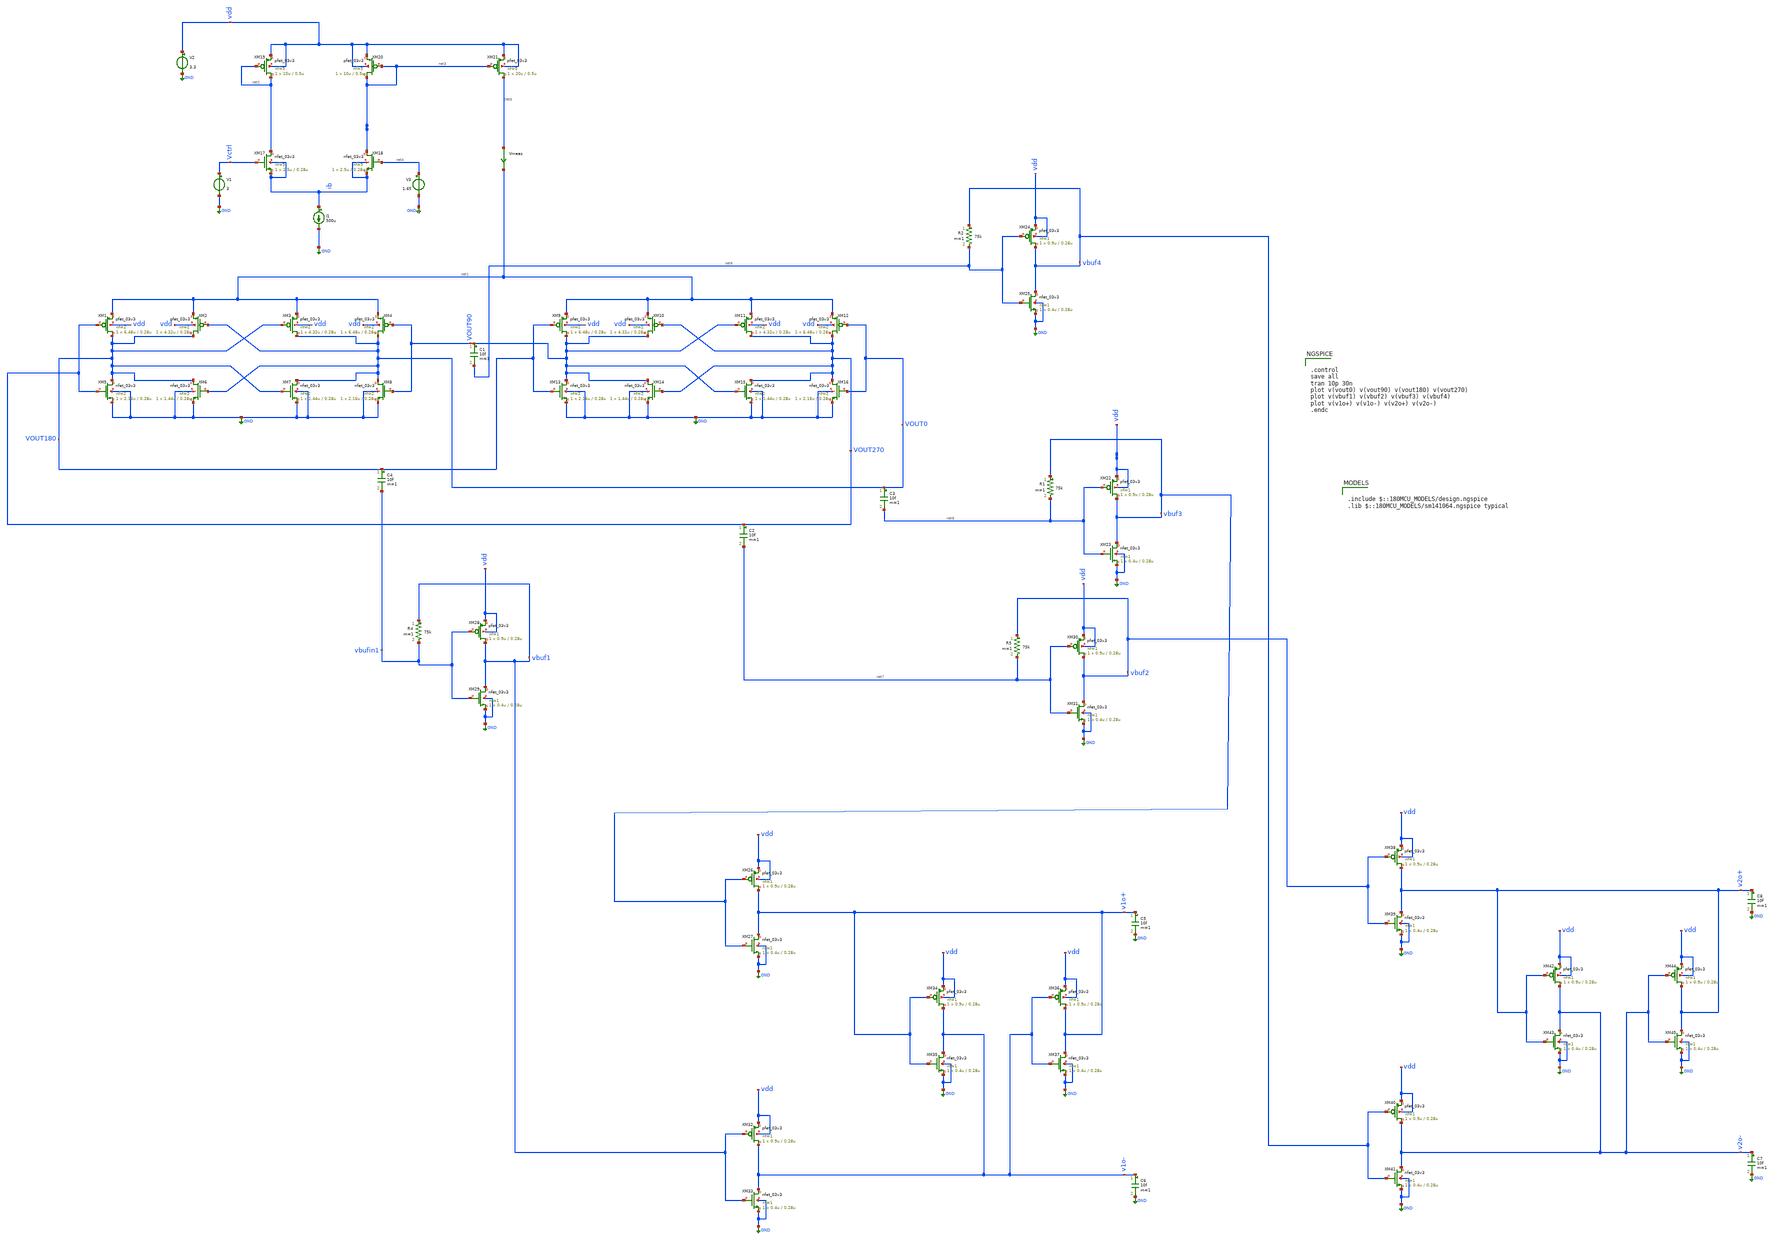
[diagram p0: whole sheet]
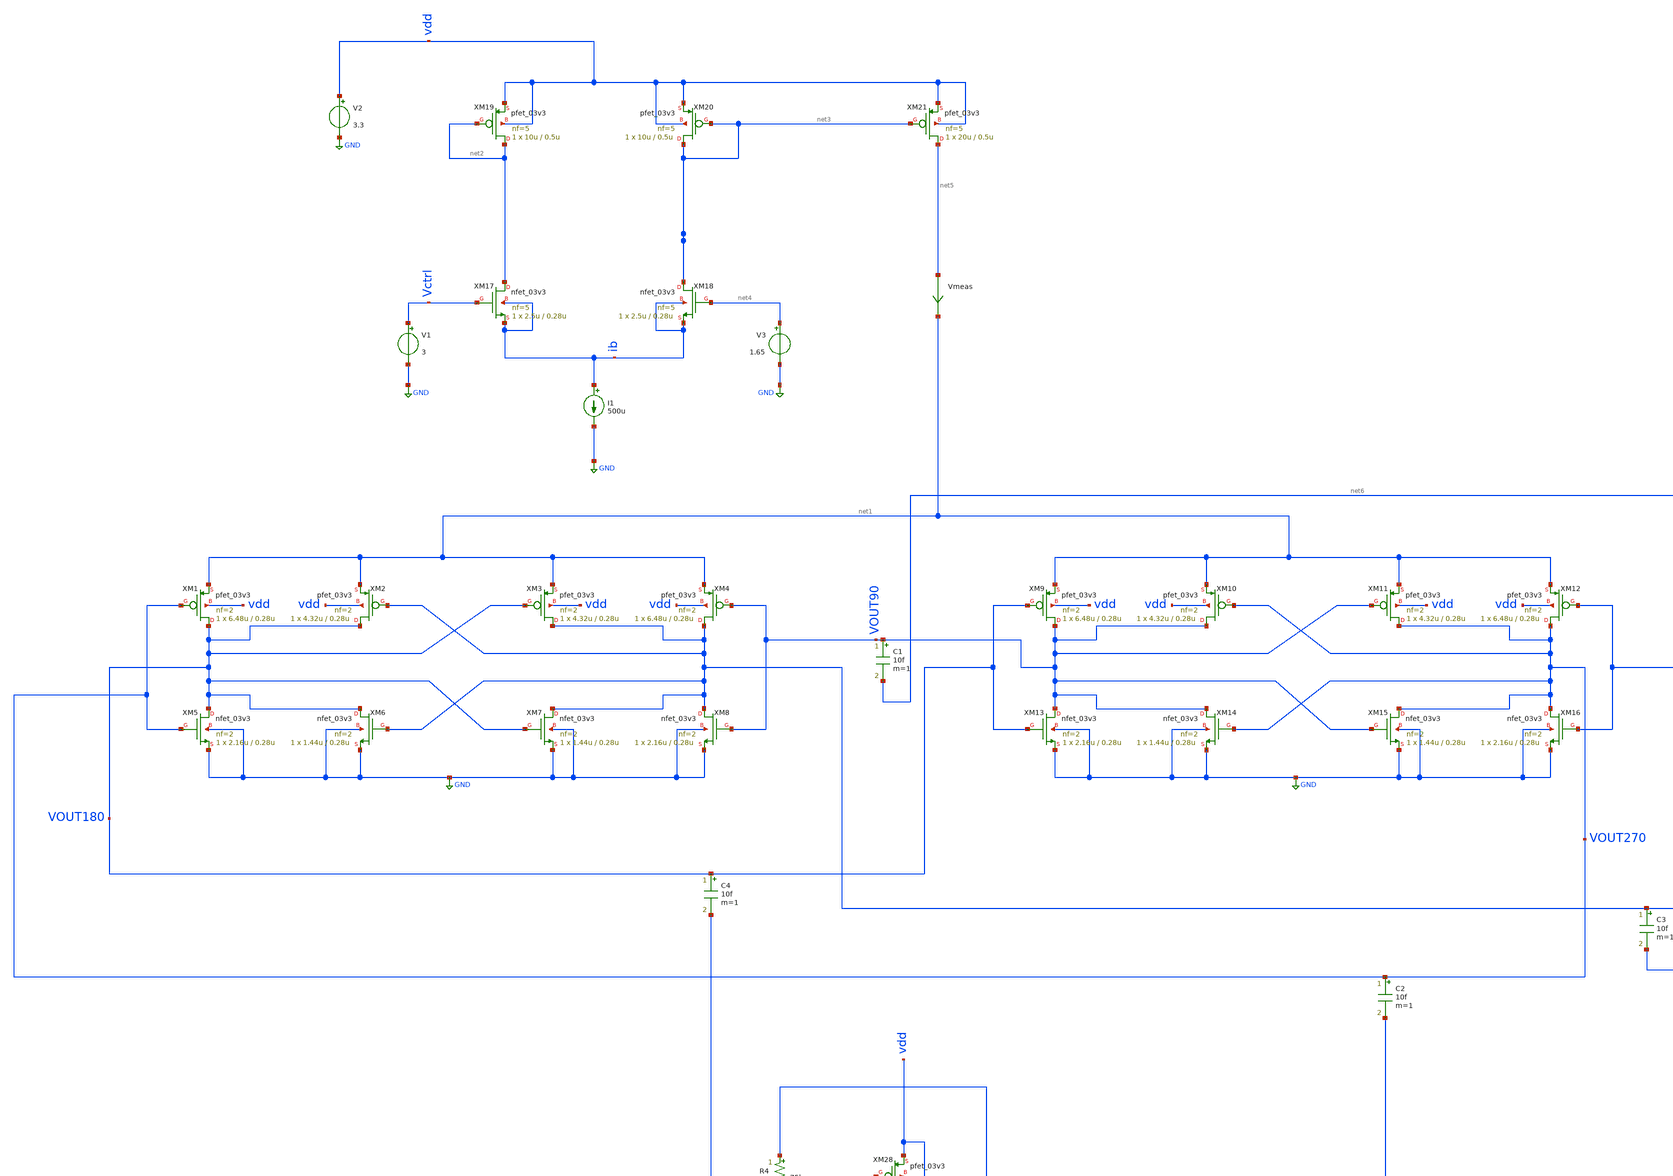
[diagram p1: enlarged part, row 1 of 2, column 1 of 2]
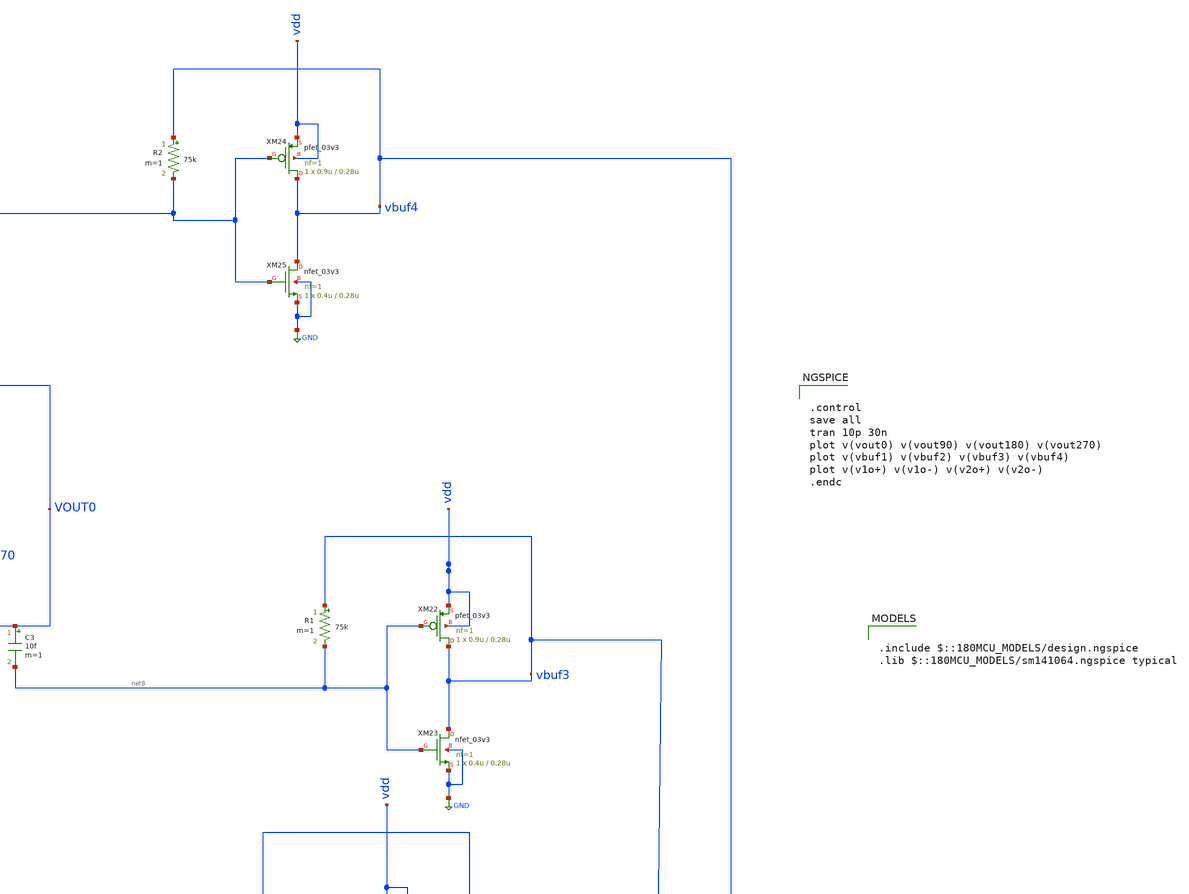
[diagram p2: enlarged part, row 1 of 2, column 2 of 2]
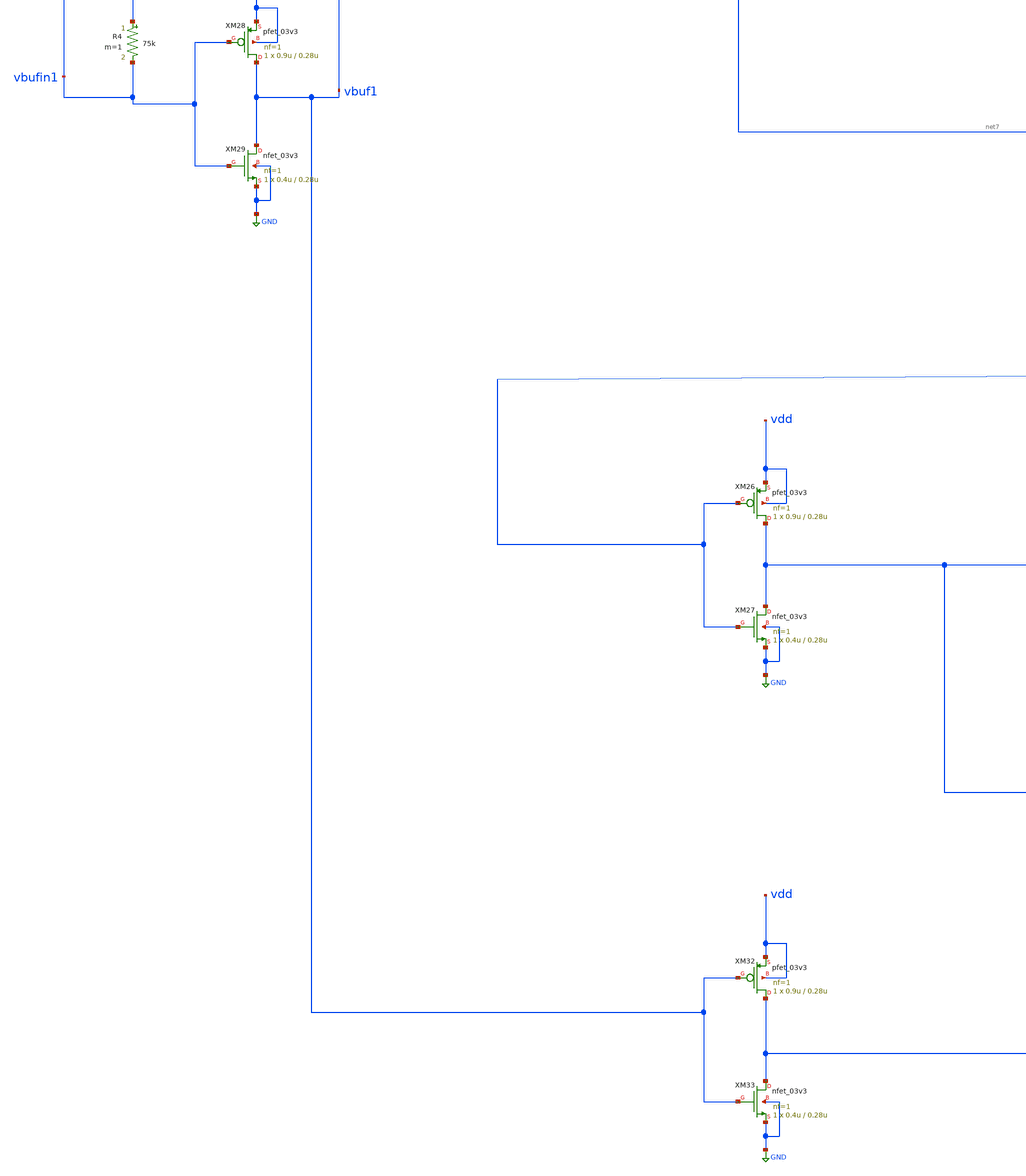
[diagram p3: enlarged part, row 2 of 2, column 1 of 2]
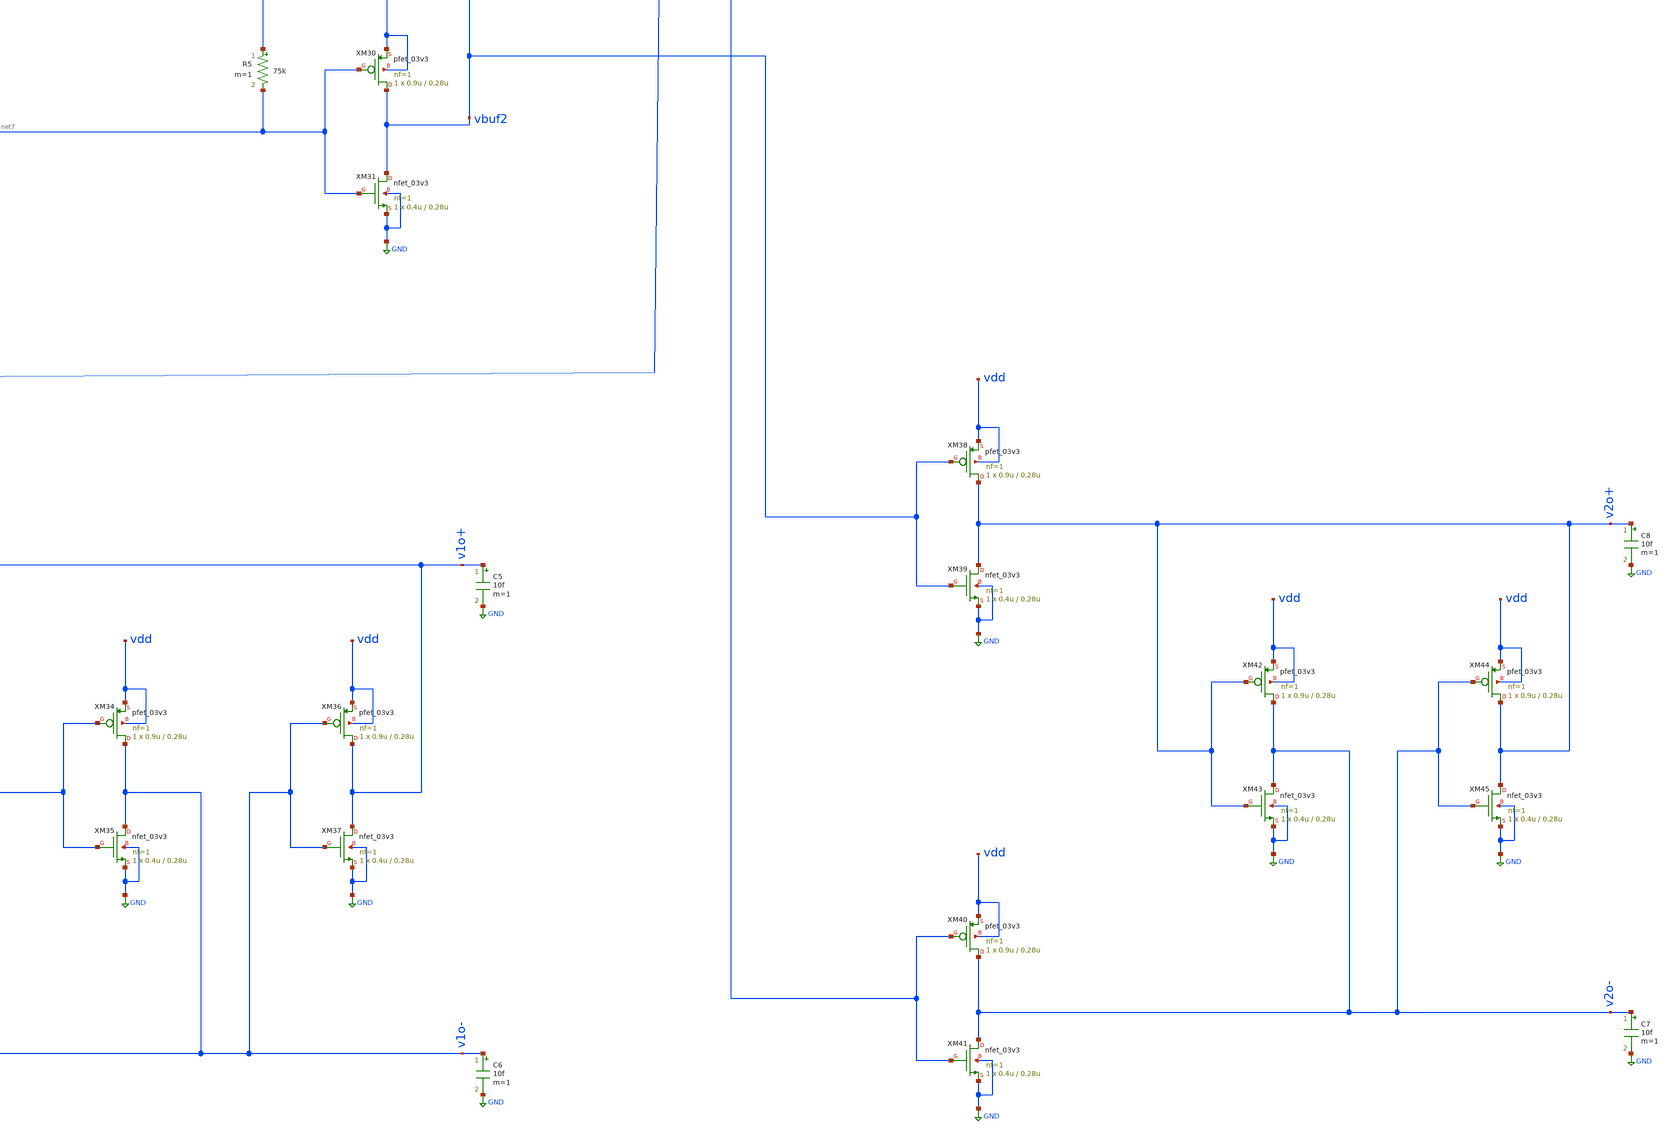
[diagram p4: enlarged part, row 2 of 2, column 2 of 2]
** sch_path: xschem/delay_tb.sch
**.subckt delay_tb
XM1 VOUT180 VOUT270 net1 vdd pfet_03v3 L=0.28u W=6.48u nf=2 ad='int((nf+1)/2) * W/nf * 0.18u' as='int((nf+2)/2) * W/nf * 0.18u'
+ pd='2*int((nf+1)/2) * (W/nf + 0.18u)' ps='2*int((nf+2)/2) * (W/nf + 0.18u)' nrd='0.18u / W' nrs='0.18u / W'
+ sa=0 sb=0 sd=0 m=1
XM2 VOUT180 VOUT0 net1 vdd pfet_03v3 L=0.28u W=4.32u nf=2 ad='int((nf+1)/2) * W/nf * 0.18u' as='int((nf+2)/2) * W/nf * 0.18u'
+ pd='2*int((nf+1)/2) * (W/nf + 0.18u)' ps='2*int((nf+2)/2) * (W/nf + 0.18u)' nrd='0.18u / W' nrs='0.18u / W'
+ sa=0 sb=0 sd=0 m=1
XM3 VOUT0 VOUT180 net1 vdd pfet_03v3 L=0.28u W=4.32u nf=2 ad='int((nf+1)/2) * W/nf * 0.18u' as='int((nf+2)/2) * W/nf * 0.18u'
+ pd='2*int((nf+1)/2) * (W/nf + 0.18u)' ps='2*int((nf+2)/2) * (W/nf + 0.18u)' nrd='0.18u / W' nrs='0.18u / W'
+ sa=0 sb=0 sd=0 m=1
XM4 VOUT0 VOUT90 net1 vdd pfet_03v3 L=0.28u W=6.48u nf=2 ad='int((nf+1)/2) * W/nf * 0.18u' as='int((nf+2)/2) * W/nf * 0.18u'
+ pd='2*int((nf+1)/2) * (W/nf + 0.18u)' ps='2*int((nf+2)/2) * (W/nf + 0.18u)' nrd='0.18u / W' nrs='0.18u / W'
+ sa=0 sb=0 sd=0 m=1
XM5 VOUT180 VOUT270 GND GND nfet_03v3 L=0.28u W=2.16u nf=2 ad='int((nf+1)/2) * W/nf * 0.18u' as='int((nf+2)/2) * W/nf * 0.18u'
+ pd='2*int((nf+1)/2) * (W/nf + 0.18u)' ps='2*int((nf+2)/2) * (W/nf + 0.18u)' nrd='0.18u / W' nrs='0.18u / W'
+ sa=0 sb=0 sd=0 m=1
XM6 VOUT180 VOUT0 GND GND nfet_03v3 L=0.28u W=1.44u nf=2 ad='int((nf+1)/2) * W/nf * 0.18u' as='int((nf+2)/2) * W/nf * 0.18u'
+ pd='2*int((nf+1)/2) * (W/nf + 0.18u)' ps='2*int((nf+2)/2) * (W/nf + 0.18u)' nrd='0.18u / W' nrs='0.18u / W'
+ sa=0 sb=0 sd=0 m=1
XM7 VOUT0 VOUT180 GND GND nfet_03v3 L=0.28u W=1.44u nf=2 ad='int((nf+1)/2) * W/nf * 0.18u' as='int((nf+2)/2) * W/nf * 0.18u'
+ pd='2*int((nf+1)/2) * (W/nf + 0.18u)' ps='2*int((nf+2)/2) * (W/nf + 0.18u)' nrd='0.18u / W' nrs='0.18u / W'
+ sa=0 sb=0 sd=0 m=1
XM8 VOUT0 VOUT90 GND GND nfet_03v3 L=0.28u W=2.16u nf=2 ad='int((nf+1)/2) * W/nf * 0.18u' as='int((nf+2)/2) * W/nf * 0.18u'
+ pd='2*int((nf+1)/2) * (W/nf + 0.18u)' ps='2*int((nf+2)/2) * (W/nf + 0.18u)' nrd='0.18u / W' nrs='0.18u / W'
+ sa=0 sb=0 sd=0 m=1
XM9 VOUT90 VOUT180 net1 vdd pfet_03v3 L=0.28u W=6.48u nf=2 ad='int((nf+1)/2) * W/nf * 0.18u' as='int((nf+2)/2) * W/nf * 0.18u'
+ pd='2*int((nf+1)/2) * (W/nf + 0.18u)' ps='2*int((nf+2)/2) * (W/nf + 0.18u)' nrd='0.18u / W' nrs='0.18u / W'
+ sa=0 sb=0 sd=0 m=1
XM10 VOUT90 VOUT270 net1 vdd pfet_03v3 L=0.28u W=4.32u nf=2 ad='int((nf+1)/2) * W/nf * 0.18u' as='int((nf+2)/2) * W/nf * 0.18u'
+ pd='2*int((nf+1)/2) * (W/nf + 0.18u)' ps='2*int((nf+2)/2) * (W/nf + 0.18u)' nrd='0.18u / W' nrs='0.18u / W'
+ sa=0 sb=0 sd=0 m=1
XM11 VOUT270 VOUT90 net1 vdd pfet_03v3 L=0.28u W=4.32u nf=2 ad='int((nf+1)/2) * W/nf * 0.18u' as='int((nf+2)/2) * W/nf * 0.18u'
+ pd='2*int((nf+1)/2) * (W/nf + 0.18u)' ps='2*int((nf+2)/2) * (W/nf + 0.18u)' nrd='0.18u / W' nrs='0.18u / W'
+ sa=0 sb=0 sd=0 m=1
XM12 VOUT270 VOUT0 net1 vdd pfet_03v3 L=0.28u W=6.48u nf=2 ad='int((nf+1)/2) * W/nf * 0.18u' as='int((nf+2)/2) * W/nf * 0.18u'
+ pd='2*int((nf+1)/2) * (W/nf + 0.18u)' ps='2*int((nf+2)/2) * (W/nf + 0.18u)' nrd='0.18u / W' nrs='0.18u / W'
+ sa=0 sb=0 sd=0 m=1
XM13 VOUT90 VOUT180 GND GND nfet_03v3 L=0.28u W=2.16u nf=2 ad='int((nf+1)/2) * W/nf * 0.18u' as='int((nf+2)/2) * W/nf * 0.18u'
+ pd='2*int((nf+1)/2) * (W/nf + 0.18u)' ps='2*int((nf+2)/2) * (W/nf + 0.18u)' nrd='0.18u / W' nrs='0.18u / W'
+ sa=0 sb=0 sd=0 m=1
XM14 VOUT90 VOUT270 GND GND nfet_03v3 L=0.28u W=1.44u nf=2 ad='int((nf+1)/2) * W/nf * 0.18u' as='int((nf+2)/2) * W/nf * 0.18u'
+ pd='2*int((nf+1)/2) * (W/nf + 0.18u)' ps='2*int((nf+2)/2) * (W/nf + 0.18u)' nrd='0.18u / W' nrs='0.18u / W'
+ sa=0 sb=0 sd=0 m=1
XM15 VOUT270 VOUT90 GND GND nfet_03v3 L=0.28u W=1.44u nf=2 ad='int((nf+1)/2) * W/nf * 0.18u' as='int((nf+2)/2) * W/nf * 0.18u'
+ pd='2*int((nf+1)/2) * (W/nf + 0.18u)' ps='2*int((nf+2)/2) * (W/nf + 0.18u)' nrd='0.18u / W' nrs='0.18u / W'
+ sa=0 sb=0 sd=0 m=1
XM16 VOUT270 VOUT0 GND GND nfet_03v3 L=0.28u W=2.16u nf=2 ad='int((nf+1)/2) * W/nf * 0.18u' as='int((nf+2)/2) * W/nf * 0.18u'
+ pd='2*int((nf+1)/2) * (W/nf + 0.18u)' ps='2*int((nf+2)/2) * (W/nf + 0.18u)' nrd='0.18u / W' nrs='0.18u / W'
+ sa=0 sb=0 sd=0 m=1
V1 Vctrl GND 3
V2 vdd GND 3.3
I1 ib GND 500u
V3 net4 GND 1.65
XM17 net2 Vctrl ib ib nfet_03v3 L=0.28u W=2.5u nf=5 ad='int((nf+1)/2) * W/nf * 0.18u' as='int((nf+2)/2) * W/nf * 0.18u'
+ pd='2*int((nf+1)/2) * (W/nf + 0.18u)' ps='2*int((nf+2)/2) * (W/nf + 0.18u)' nrd='0.18u / W' nrs='0.18u / W'
+ sa=0 sb=0 sd=0 m=1
XM18 net3 net4 ib ib nfet_03v3 L=0.28u W=2.5u nf=5 ad='int((nf+1)/2) * W/nf * 0.18u' as='int((nf+2)/2) * W/nf * 0.18u'
+ pd='2*int((nf+1)/2) * (W/nf + 0.18u)' ps='2*int((nf+2)/2) * (W/nf + 0.18u)' nrd='0.18u / W' nrs='0.18u / W'
+ sa=0 sb=0 sd=0 m=1
XM19 net2 net2 vdd vdd pfet_03v3 L=0.5u W=10u nf=5 ad='int((nf+1)/2) * W/nf * 0.18u' as='int((nf+2)/2) * W/nf * 0.18u'
+ pd='2*int((nf+1)/2) * (W/nf + 0.18u)' ps='2*int((nf+2)/2) * (W/nf + 0.18u)' nrd='0.18u / W' nrs='0.18u / W'
+ sa=0 sb=0 sd=0 m=1
XM20 net3 net3 vdd vdd pfet_03v3 L=0.5u W=10u nf=5 ad='int((nf+1)/2) * W/nf * 0.18u' as='int((nf+2)/2) * W/nf * 0.18u'
+ pd='2*int((nf+1)/2) * (W/nf + 0.18u)' ps='2*int((nf+2)/2) * (W/nf + 0.18u)' nrd='0.18u / W' nrs='0.18u / W'
+ sa=0 sb=0 sd=0 m=1
Vmeas net5 net1 0
.save i(vmeas)
XM21 net5 net3 vdd vdd pfet_03v3 L=0.5u W=20u nf=5 ad='int((nf+1)/2) * W/nf * 0.18u' as='int((nf+2)/2) * W/nf * 0.18u'
+ pd='2*int((nf+1)/2) * (W/nf + 0.18u)' ps='2*int((nf+2)/2) * (W/nf + 0.18u)' nrd='0.18u / W' nrs='0.18u / W'
+ sa=0 sb=0 sd=0 m=1
C1 VOUT90 net6 10f m=1
C2 VOUT270 net7 10f m=1
C3 VOUT0 net8 10f m=1
C4 VOUT180 vbufin1 10f m=1
XM28 vbuf1 vbufin1 vdd vdd pfet_03v3 L=0.28u W=0.9u nf=1 ad='int((nf+1)/2) * W/nf * 0.18u' as='int((nf+2)/2) * W/nf * 0.18u'
+ pd='2*int((nf+1)/2) * (W/nf + 0.18u)' ps='2*int((nf+2)/2) * (W/nf + 0.18u)' nrd='0.18u / W' nrs='0.18u / W'
+ sa=0 sb=0 sd=0 m=1
XM29 vbuf1 vbufin1 GND GND nfet_03v3 L=0.28u W=0.4u nf=1 ad='int((nf+1)/2) * W/nf * 0.18u' as='int((nf+2)/2) * W/nf * 0.18u'
+ pd='2*int((nf+1)/2) * (W/nf + 0.18u)' ps='2*int((nf+2)/2) * (W/nf + 0.18u)' nrd='0.18u / W' nrs='0.18u / W'
+ sa=0 sb=0 sd=0 m=1
R4 vbuf1 vbufin1 75k m=1
XM30 vbuf2 net7 vdd vdd pfet_03v3 L=0.28u W=0.9u nf=1 ad='int((nf+1)/2) * W/nf * 0.18u' as='int((nf+2)/2) * W/nf * 0.18u'
+ pd='2*int((nf+1)/2) * (W/nf + 0.18u)' ps='2*int((nf+2)/2) * (W/nf + 0.18u)' nrd='0.18u / W' nrs='0.18u / W'
+ sa=0 sb=0 sd=0 m=1
XM31 vbuf2 net7 GND GND nfet_03v3 L=0.28u W=0.4u nf=1 ad='int((nf+1)/2) * W/nf * 0.18u' as='int((nf+2)/2) * W/nf * 0.18u'
+ pd='2*int((nf+1)/2) * (W/nf + 0.18u)' ps='2*int((nf+2)/2) * (W/nf + 0.18u)' nrd='0.18u / W' nrs='0.18u / W'
+ sa=0 sb=0 sd=0 m=1
R5 vbuf2 net7 75k m=1
XM22 vbuf3 net8 vdd vdd pfet_03v3 L=0.28u W=0.9u nf=1 ad='int((nf+1)/2) * W/nf * 0.18u' as='int((nf+2)/2) * W/nf * 0.18u'
+ pd='2*int((nf+1)/2) * (W/nf + 0.18u)' ps='2*int((nf+2)/2) * (W/nf + 0.18u)' nrd='0.18u / W' nrs='0.18u / W'
+ sa=0 sb=0 sd=0 m=1
XM23 vbuf3 net8 GND GND nfet_03v3 L=0.28u W=0.4u nf=1 ad='int((nf+1)/2) * W/nf * 0.18u' as='int((nf+2)/2) * W/nf * 0.18u'
+ pd='2*int((nf+1)/2) * (W/nf + 0.18u)' ps='2*int((nf+2)/2) * (W/nf + 0.18u)' nrd='0.18u / W' nrs='0.18u / W'
+ sa=0 sb=0 sd=0 m=1
R1 vbuf3 net8 75k m=1
XM24 vbuf4 net6 vdd vdd pfet_03v3 L=0.28u W=0.9u nf=1 ad='int((nf+1)/2) * W/nf * 0.18u' as='int((nf+2)/2) * W/nf * 0.18u'
+ pd='2*int((nf+1)/2) * (W/nf + 0.18u)' ps='2*int((nf+2)/2) * (W/nf + 0.18u)' nrd='0.18u / W' nrs='0.18u / W'
+ sa=0 sb=0 sd=0 m=1
XM25 vbuf4 net6 GND GND nfet_03v3 L=0.28u W=0.4u nf=1 ad='int((nf+1)/2) * W/nf * 0.18u' as='int((nf+2)/2) * W/nf * 0.18u'
+ pd='2*int((nf+1)/2) * (W/nf + 0.18u)' ps='2*int((nf+2)/2) * (W/nf + 0.18u)' nrd='0.18u / W' nrs='0.18u / W'
+ sa=0 sb=0 sd=0 m=1
R2 vbuf4 net6 75k m=1
XM26 v1o+ vbuf3 vdd vdd pfet_03v3 L=0.28u W=0.9u nf=1 ad='int((nf+1)/2) * W/nf * 0.18u' as='int((nf+2)/2) * W/nf * 0.18u'
+ pd='2*int((nf+1)/2) * (W/nf + 0.18u)' ps='2*int((nf+2)/2) * (W/nf + 0.18u)' nrd='0.18u / W' nrs='0.18u / W'
+ sa=0 sb=0 sd=0 m=1
XM27 v1o+ vbuf3 GND GND nfet_03v3 L=0.28u W=0.4u nf=1 ad='int((nf+1)/2) * W/nf * 0.18u' as='int((nf+2)/2) * W/nf * 0.18u'
+ pd='2*int((nf+1)/2) * (W/nf + 0.18u)' ps='2*int((nf+2)/2) * (W/nf + 0.18u)' nrd='0.18u / W' nrs='0.18u / W'
+ sa=0 sb=0 sd=0 m=1
XM32 v1o- vbuf1 vdd vdd pfet_03v3 L=0.28u W=0.9u nf=1 ad='int((nf+1)/2) * W/nf * 0.18u' as='int((nf+2)/2) * W/nf * 0.18u'
+ pd='2*int((nf+1)/2) * (W/nf + 0.18u)' ps='2*int((nf+2)/2) * (W/nf + 0.18u)' nrd='0.18u / W' nrs='0.18u / W'
+ sa=0 sb=0 sd=0 m=1
XM33 v1o- vbuf1 GND GND nfet_03v3 L=0.28u W=0.4u nf=1 ad='int((nf+1)/2) * W/nf * 0.18u' as='int((nf+2)/2) * W/nf * 0.18u'
+ pd='2*int((nf+1)/2) * (W/nf + 0.18u)' ps='2*int((nf+2)/2) * (W/nf + 0.18u)' nrd='0.18u / W' nrs='0.18u / W'
+ sa=0 sb=0 sd=0 m=1
XM34 v1o- v1o+ vdd vdd pfet_03v3 L=0.28u W=0.9u nf=1 ad='int((nf+1)/2) * W/nf * 0.18u' as='int((nf+2)/2) * W/nf * 0.18u'
+ pd='2*int((nf+1)/2) * (W/nf + 0.18u)' ps='2*int((nf+2)/2) * (W/nf + 0.18u)' nrd='0.18u / W' nrs='0.18u / W'
+ sa=0 sb=0 sd=0 m=1
XM35 v1o- v1o+ GND GND nfet_03v3 L=0.28u W=0.4u nf=1 ad='int((nf+1)/2) * W/nf * 0.18u' as='int((nf+2)/2) * W/nf * 0.18u'
+ pd='2*int((nf+1)/2) * (W/nf + 0.18u)' ps='2*int((nf+2)/2) * (W/nf + 0.18u)' nrd='0.18u / W' nrs='0.18u / W'
+ sa=0 sb=0 sd=0 m=1
XM36 v1o+ v1o- vdd vdd pfet_03v3 L=0.28u W=0.9u nf=1 ad='int((nf+1)/2) * W/nf * 0.18u' as='int((nf+2)/2) * W/nf * 0.18u'
+ pd='2*int((nf+1)/2) * (W/nf + 0.18u)' ps='2*int((nf+2)/2) * (W/nf + 0.18u)' nrd='0.18u / W' nrs='0.18u / W'
+ sa=0 sb=0 sd=0 m=1
XM37 v1o+ v1o- GND GND nfet_03v3 L=0.28u W=0.4u nf=1 ad='int((nf+1)/2) * W/nf * 0.18u' as='int((nf+2)/2) * W/nf * 0.18u'
+ pd='2*int((nf+1)/2) * (W/nf + 0.18u)' ps='2*int((nf+2)/2) * (W/nf + 0.18u)' nrd='0.18u / W' nrs='0.18u / W'
+ sa=0 sb=0 sd=0 m=1
XM38 v2o+ vbuf2 vdd vdd pfet_03v3 L=0.28u W=0.9u nf=1 ad='int((nf+1)/2) * W/nf * 0.18u' as='int((nf+2)/2) * W/nf * 0.18u'
+ pd='2*int((nf+1)/2) * (W/nf + 0.18u)' ps='2*int((nf+2)/2) * (W/nf + 0.18u)' nrd='0.18u / W' nrs='0.18u / W'
+ sa=0 sb=0 sd=0 m=1
XM39 v2o+ vbuf2 GND GND nfet_03v3 L=0.28u W=0.4u nf=1 ad='int((nf+1)/2) * W/nf * 0.18u' as='int((nf+2)/2) * W/nf * 0.18u'
+ pd='2*int((nf+1)/2) * (W/nf + 0.18u)' ps='2*int((nf+2)/2) * (W/nf + 0.18u)' nrd='0.18u / W' nrs='0.18u / W'
+ sa=0 sb=0 sd=0 m=1
XM40 v2o- vbuf4 vdd vdd pfet_03v3 L=0.28u W=0.9u nf=1 ad='int((nf+1)/2) * W/nf * 0.18u' as='int((nf+2)/2) * W/nf * 0.18u'
+ pd='2*int((nf+1)/2) * (W/nf + 0.18u)' ps='2*int((nf+2)/2) * (W/nf + 0.18u)' nrd='0.18u / W' nrs='0.18u / W'
+ sa=0 sb=0 sd=0 m=1
XM41 v2o- vbuf4 GND GND nfet_03v3 L=0.28u W=0.4u nf=1 ad='int((nf+1)/2) * W/nf * 0.18u' as='int((nf+2)/2) * W/nf * 0.18u'
+ pd='2*int((nf+1)/2) * (W/nf + 0.18u)' ps='2*int((nf+2)/2) * (W/nf + 0.18u)' nrd='0.18u / W' nrs='0.18u / W'
+ sa=0 sb=0 sd=0 m=1
XM42 v2o- v2o+ vdd vdd pfet_03v3 L=0.28u W=0.9u nf=1 ad='int((nf+1)/2) * W/nf * 0.18u' as='int((nf+2)/2) * W/nf * 0.18u'
+ pd='2*int((nf+1)/2) * (W/nf + 0.18u)' ps='2*int((nf+2)/2) * (W/nf + 0.18u)' nrd='0.18u / W' nrs='0.18u / W'
+ sa=0 sb=0 sd=0 m=1
XM43 v2o- v2o+ GND GND nfet_03v3 L=0.28u W=0.4u nf=1 ad='int((nf+1)/2) * W/nf * 0.18u' as='int((nf+2)/2) * W/nf * 0.18u'
+ pd='2*int((nf+1)/2) * (W/nf + 0.18u)' ps='2*int((nf+2)/2) * (W/nf + 0.18u)' nrd='0.18u / W' nrs='0.18u / W'
+ sa=0 sb=0 sd=0 m=1
XM44 v2o+ v2o- vdd vdd pfet_03v3 L=0.28u W=0.9u nf=1 ad='int((nf+1)/2) * W/nf * 0.18u' as='int((nf+2)/2) * W/nf * 0.18u'
+ pd='2*int((nf+1)/2) * (W/nf + 0.18u)' ps='2*int((nf+2)/2) * (W/nf + 0.18u)' nrd='0.18u / W' nrs='0.18u / W'
+ sa=0 sb=0 sd=0 m=1
XM45 v2o+ v2o- GND GND nfet_03v3 L=0.28u W=0.4u nf=1 ad='int((nf+1)/2) * W/nf * 0.18u' as='int((nf+2)/2) * W/nf * 0.18u'
+ pd='2*int((nf+1)/2) * (W/nf + 0.18u)' ps='2*int((nf+2)/2) * (W/nf + 0.18u)' nrd='0.18u / W' nrs='0.18u / W'
+ sa=0 sb=0 sd=0 m=1
C5 v1o+ GND 10f m=1
C6 v1o- GND 10f m=1
C7 v2o- GND 10f m=1
C8 v2o+ GND 10f m=1
**** begin user architecture code

.include $::180MCU_MODELS/design.ngspice
.lib $::180MCU_MODELS/sm141064.ngspice typical



.control
save all
tran 10p 30n
plot v(vout0) v(vout90) v(vout180) v(vout270)
plot v(vbuf1) v(vbuf2) v(vbuf3) v(vbuf4)
plot v(v1o+) v(v1o-) v(v2o+) v(v2o-)
.endc


**** end user architecture code
**.ends
.GLOBAL GND
.end
